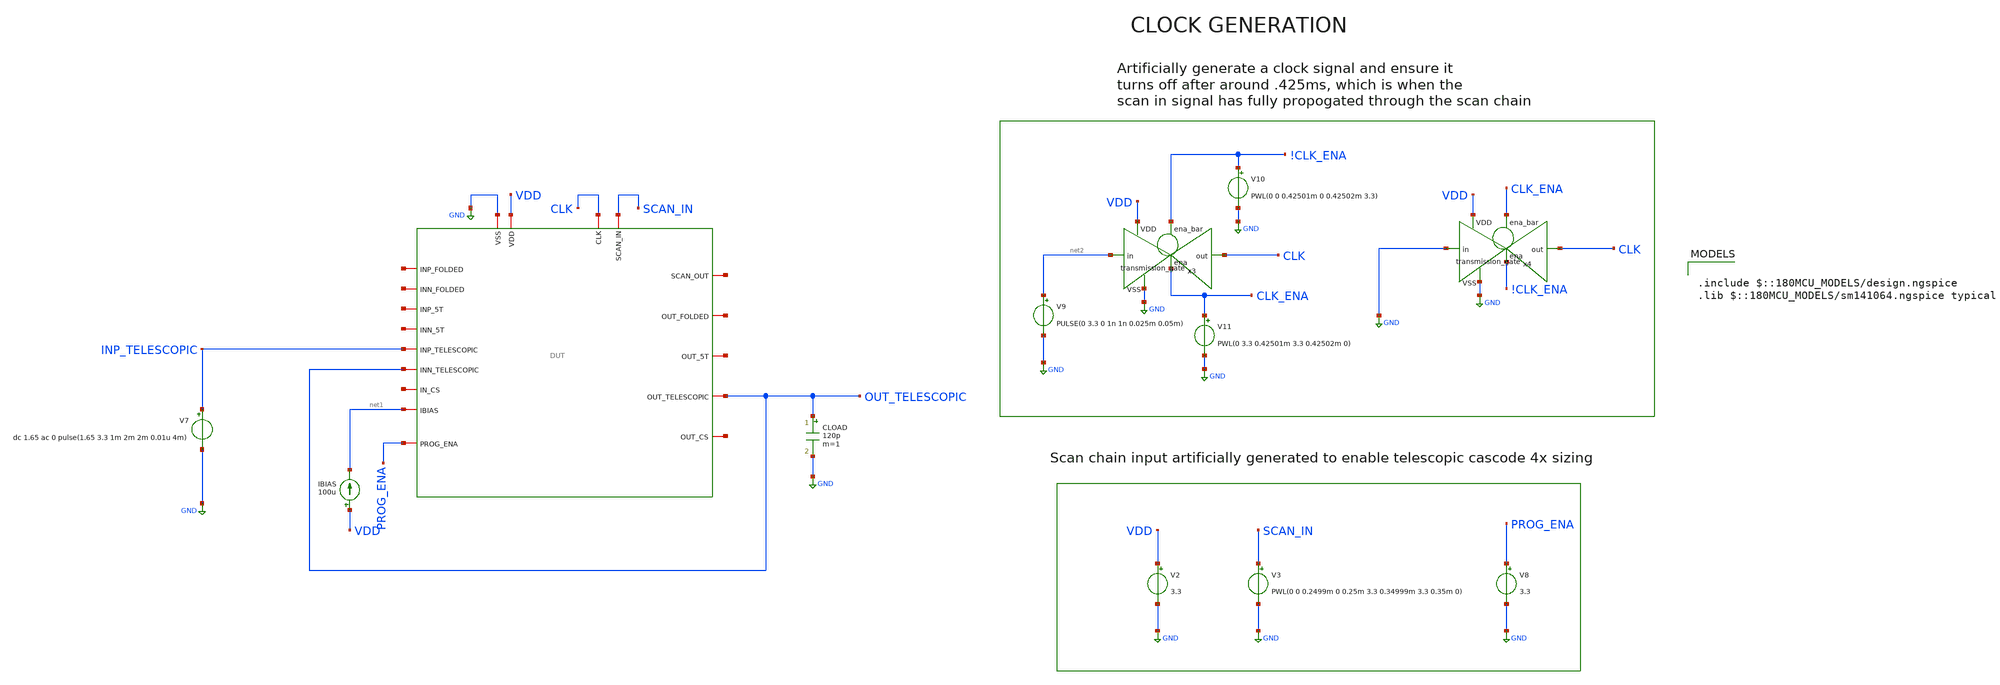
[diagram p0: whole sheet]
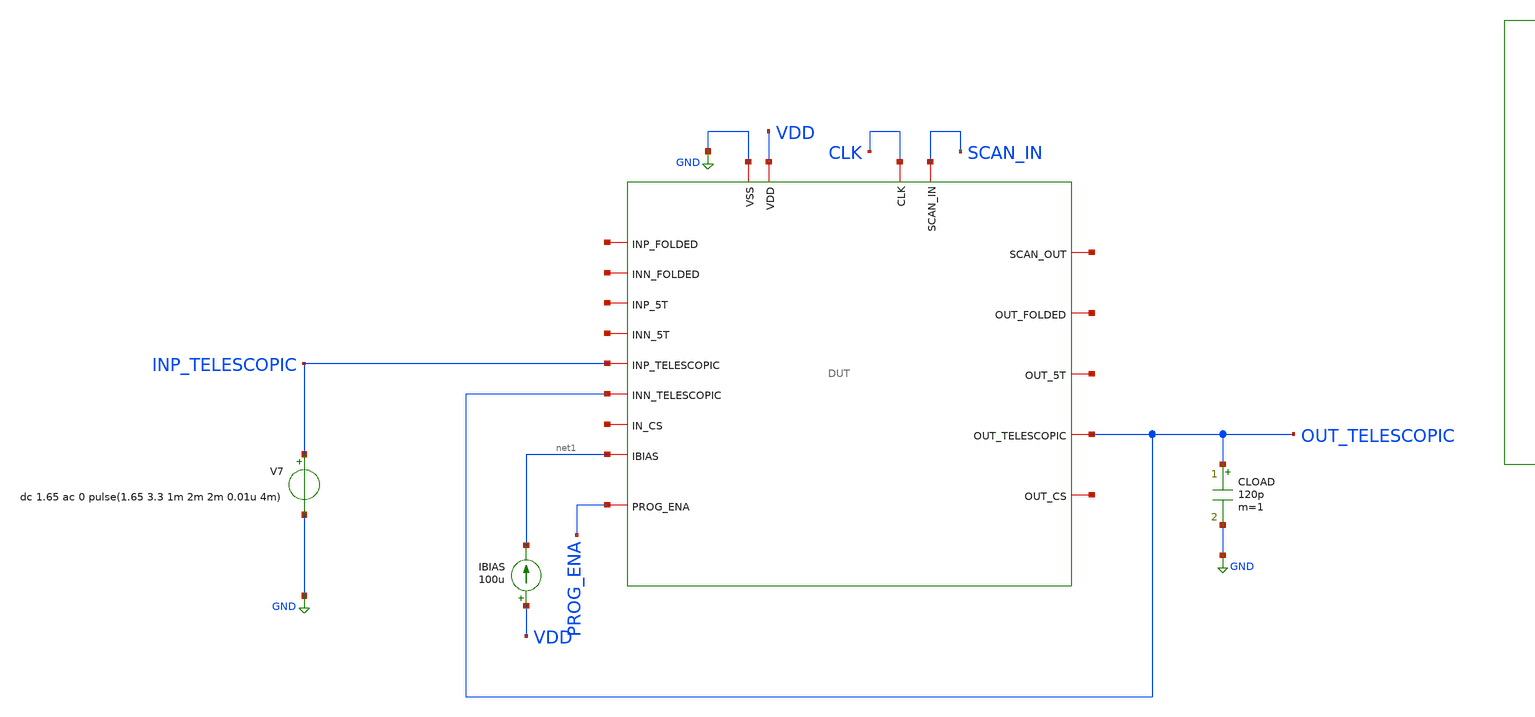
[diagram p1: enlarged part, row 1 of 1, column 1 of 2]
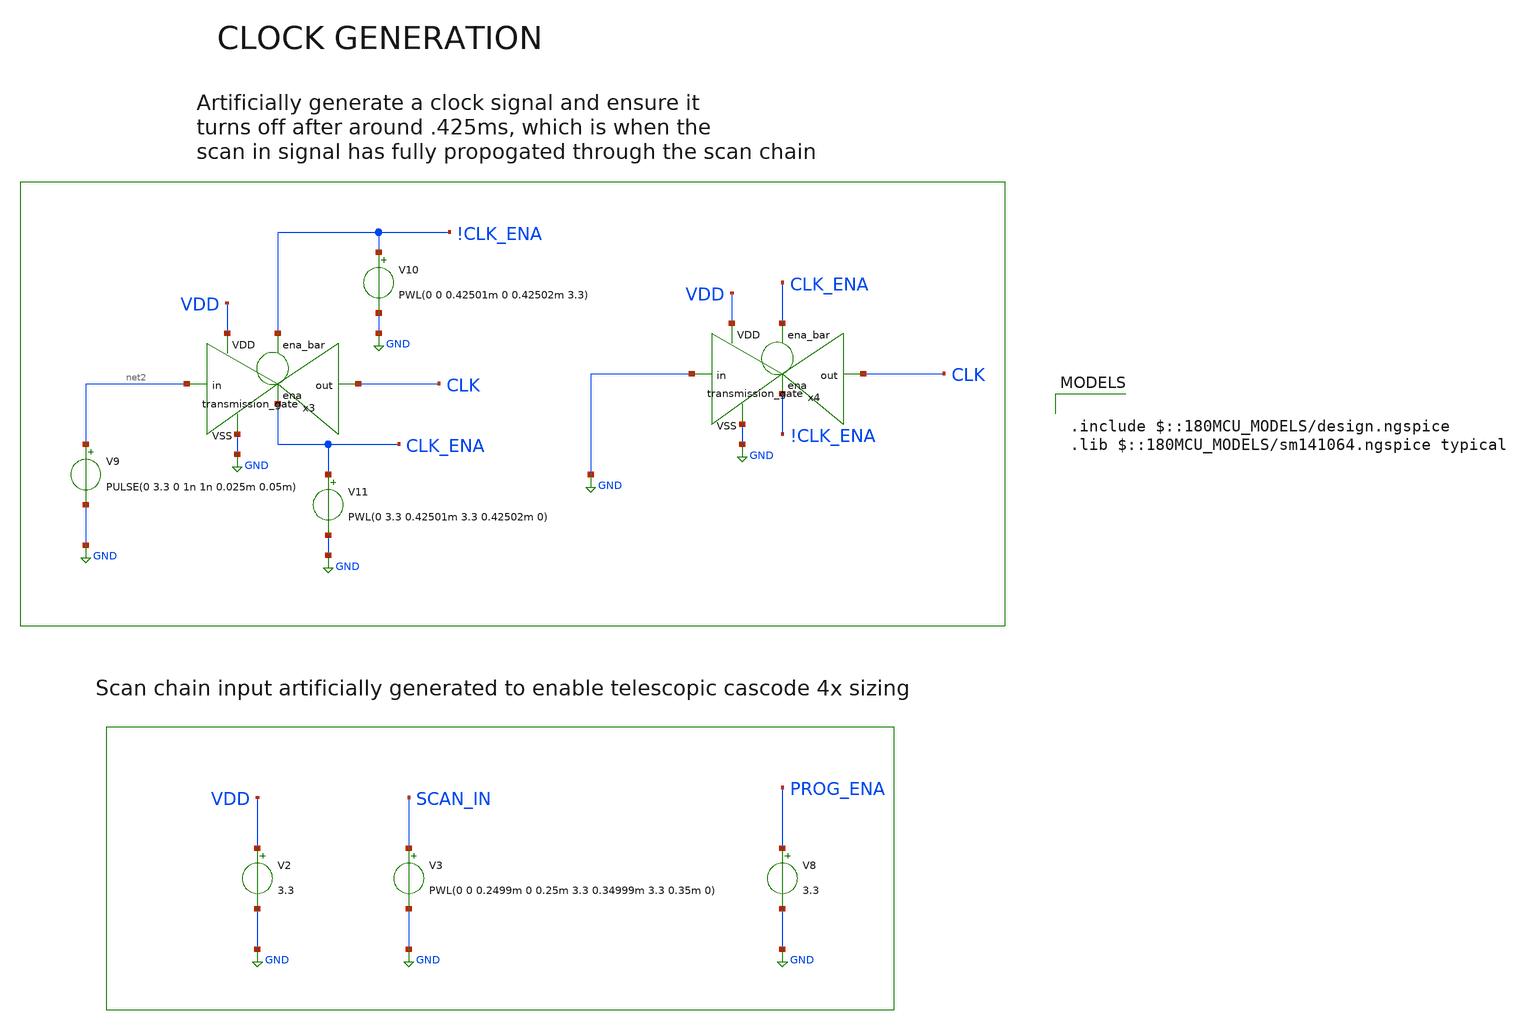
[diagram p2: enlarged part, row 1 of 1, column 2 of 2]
** sch_path: designs/libs/verification/ota_telescopic/4x/large_signal_upper_swing.sch
**.subckt large_signal_upper_swing
x1 CLK net3 SCAN_IN GND VDD net4 net5 net6 net1 net7 net8 net9 INP_TELESCOPIC OUT_TELESCOPIC net10
+ net11 OUT_TELESCOPIC PROG_ENA DUT
CLOAD OUT_TELESCOPIC GND 120p m=1
V7 INP_TELESCOPIC GND dc 1.65 ac 0 pulse(1.65 3.3 1m 2m 2m 0.01u 4m)
IBIAS VDD net1 100u
V3 SCAN_IN GND PWL(0 0 0.2499m 0 0.25m 3.3 0.34999m 3.3 0.35m 0)
V2 VDD GND 3.3
V8 PROG_ENA GND 3.3
V9 net2 GND PULSE(0 3.3 0 1n 1n 0.025m 0.05m)
x3 !CLK_ENA VDD CLK net2 GND CLK_ENA transmission_gate
V10 !CLK_ENA GND PWL(0 0 0.42501m 0 0.42502m 3.3)
V11 CLK_ENA GND PWL(0 3.3 0.42501m 3.3 0.42502m 0)
x4 CLK_ENA VDD CLK GND GND !CLK_ENA transmission_gate
**** begin user architecture code

.include $::180MCU_MODELS/design.ngspice
.lib $::180MCU_MODELS/sm141064.ngspice typical



.control
tran 1u 5m

plot v(out_telescopic) v(inp_telescopic)

let error = v(out_telescopic) - v(inp_telescopic)
plot error

meas tran t_clip when error = -0.019 cross = 1 td=.5m
print t_clip

meas tran vout_clip find v(out_telescopic) at = t_clip td=.5m
meas tran vin_clip find v(inp_telescopic) at = t_clip td=.5m
print vout_clip vin_clip
.endc


**** end user architecture code
**.ends
.GLOBAL GND
.end
